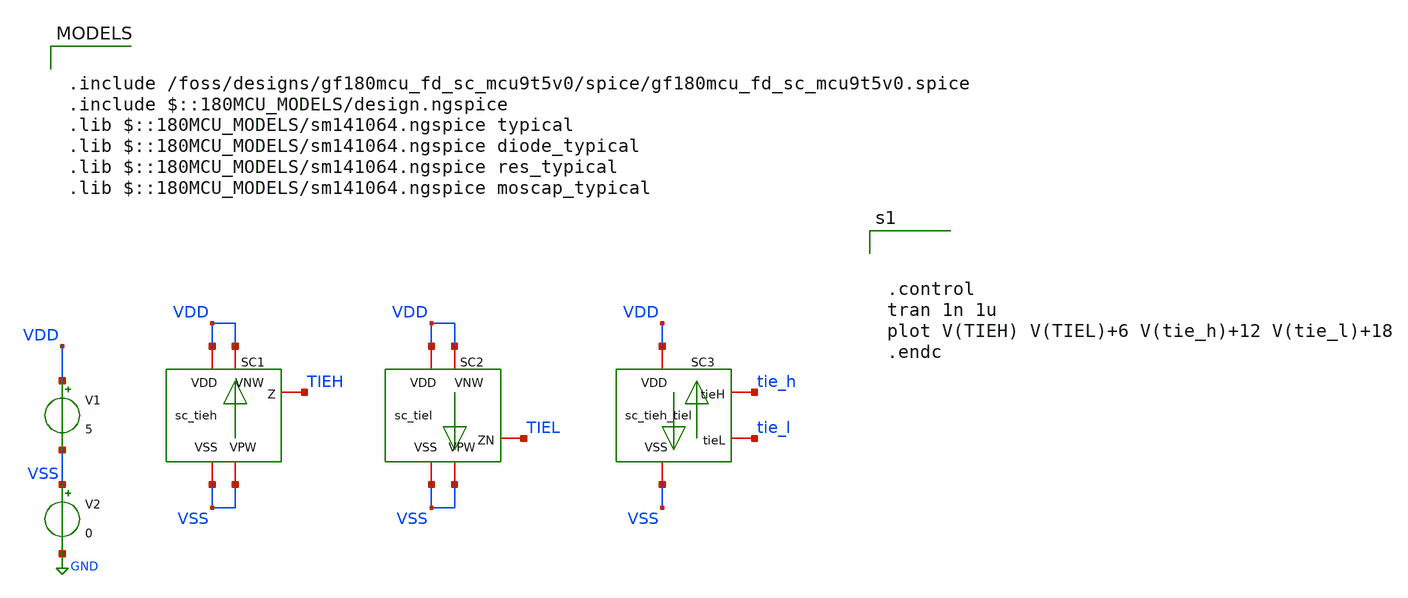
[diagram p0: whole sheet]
** sch_path: designs/gf180mcu_fd_sc_mcu9t5v0/xschem/sc_tieh_tiel_tb.sch
**.subckt sc_tieh_tiel_tb
XSC1 TIEH VDD VDD VSS VSS gf180mcu_fd_sc_mcu9t5v0__tieh
XSC2 TIEL VDD VDD VSS VSS gf180mcu_fd_sc_mcu9t5v0__tiel
V1 VDD VSS 5
V2 VSS GND 0
XSC3 tie_l VDD VSS tie_h sc_tieh_tiel
**** begin user architecture code

.include /foss/designs/gf180mcu_fd_sc_mcu9t5v0/spice/gf180mcu_fd_sc_mcu9t5v0.spice
.include $::180MCU_MODELS/design.ngspice
.lib $::180MCU_MODELS/sm141064.ngspice typical
.lib $::180MCU_MODELS/sm141064.ngspice diode_typical
.lib $::180MCU_MODELS/sm141064.ngspice res_typical
.lib $::180MCU_MODELS/sm141064.ngspice moscap_typical




.control
tran 1n 1u
plot V(TIEH) V(TIEL)+6 V(tie_h)+12 V(tie_l)+18
.endc


**** end user architecture code
**.ends
.GLOBAL GND
.end
